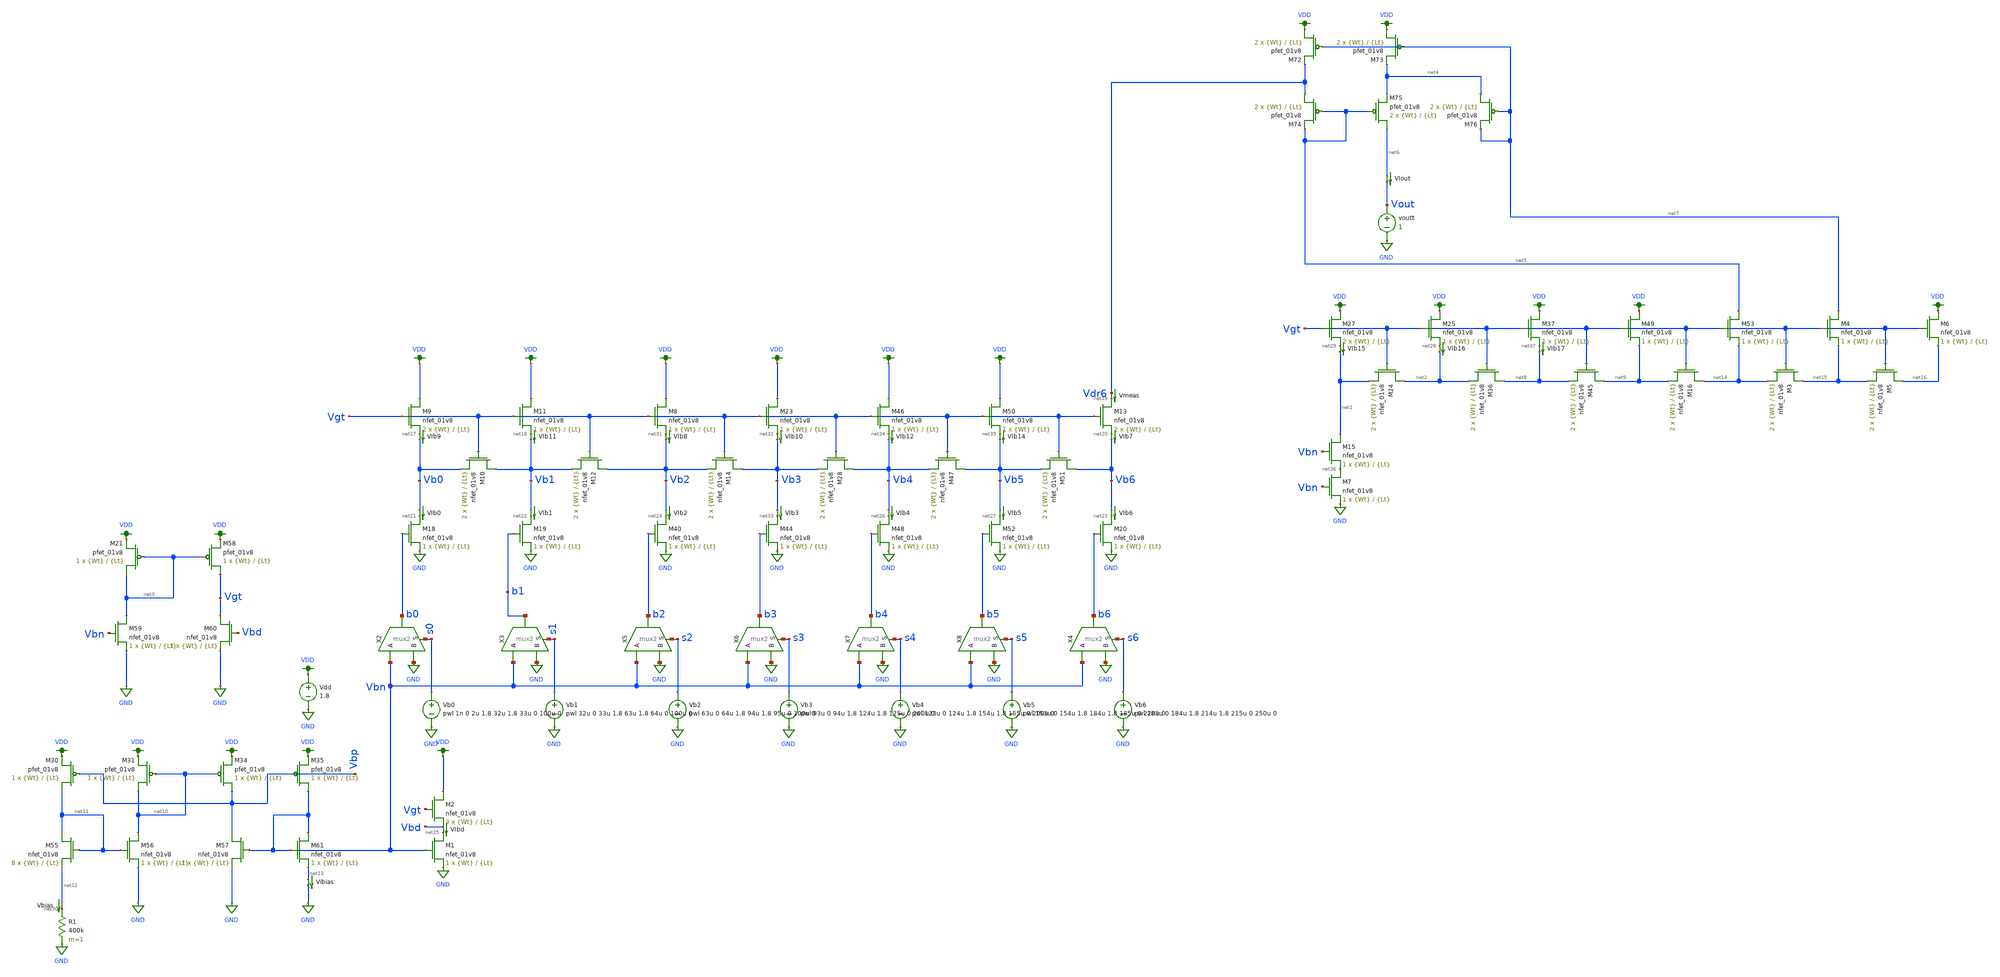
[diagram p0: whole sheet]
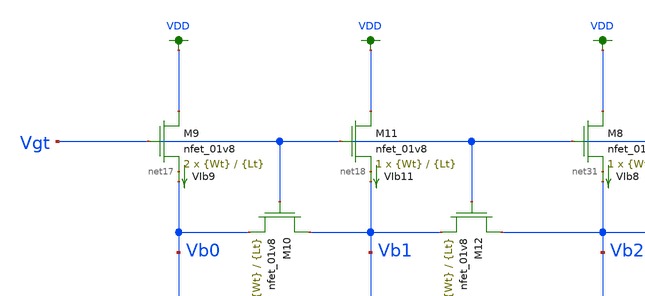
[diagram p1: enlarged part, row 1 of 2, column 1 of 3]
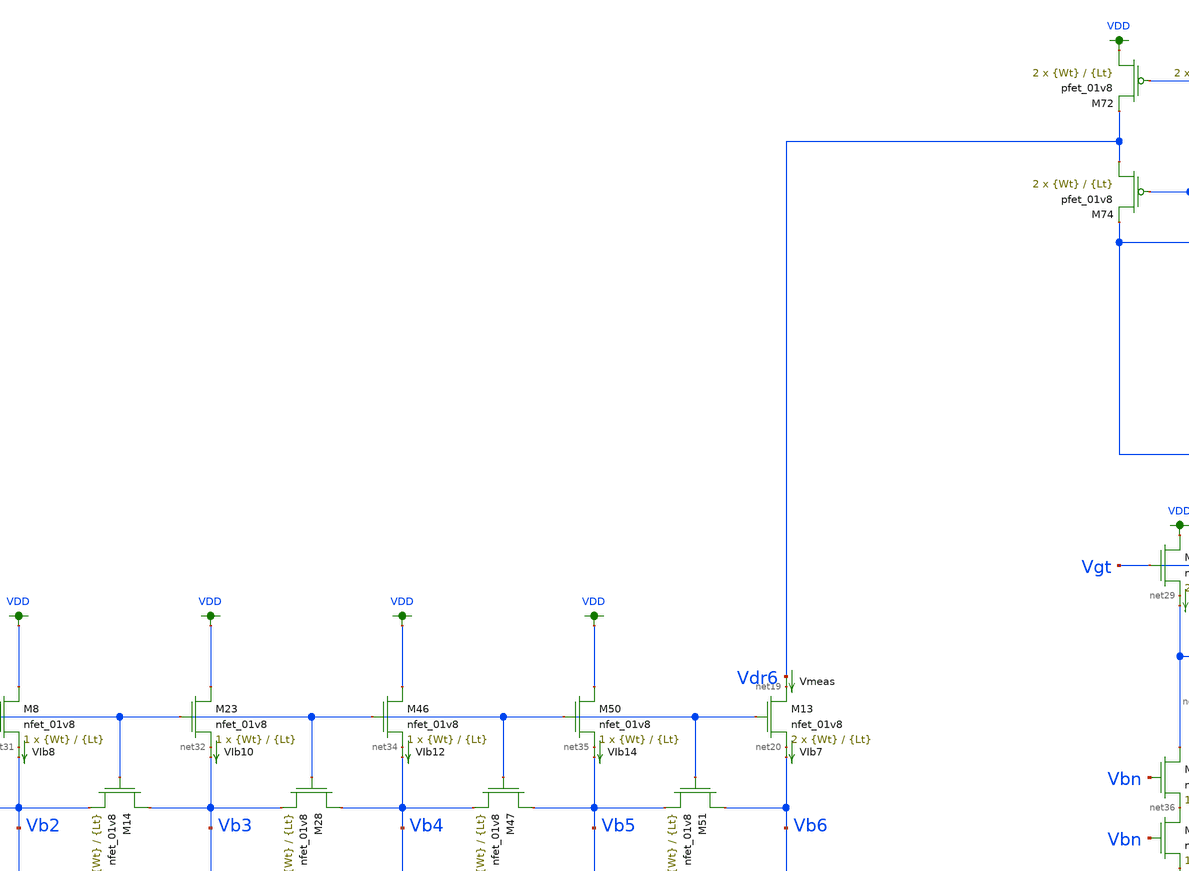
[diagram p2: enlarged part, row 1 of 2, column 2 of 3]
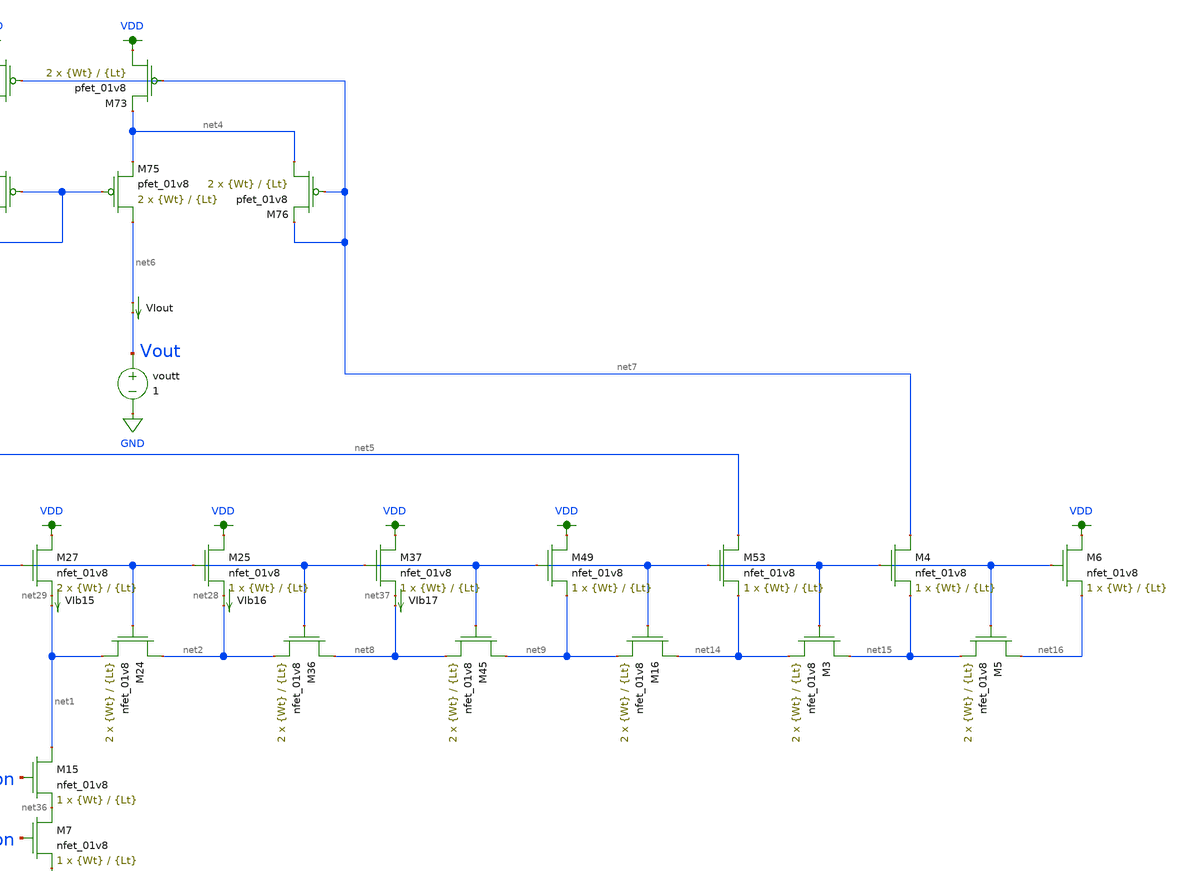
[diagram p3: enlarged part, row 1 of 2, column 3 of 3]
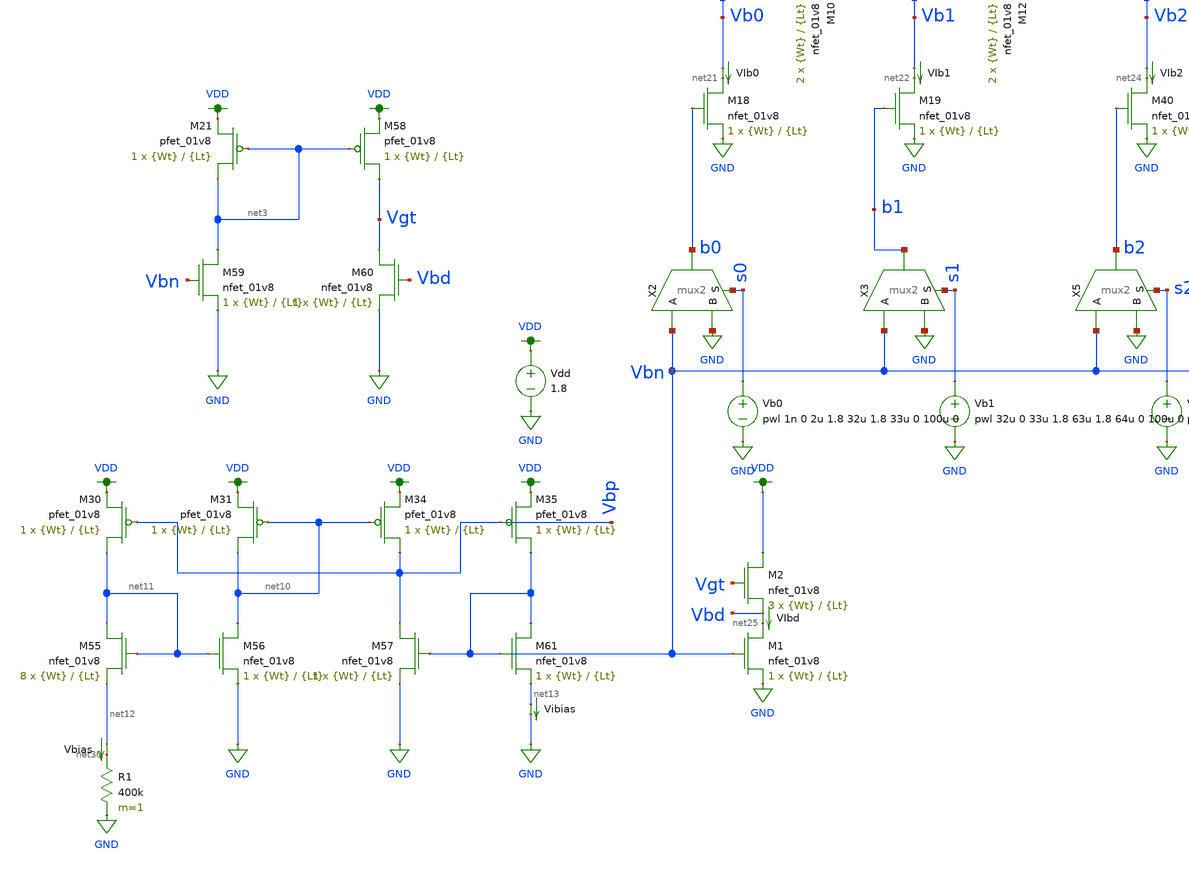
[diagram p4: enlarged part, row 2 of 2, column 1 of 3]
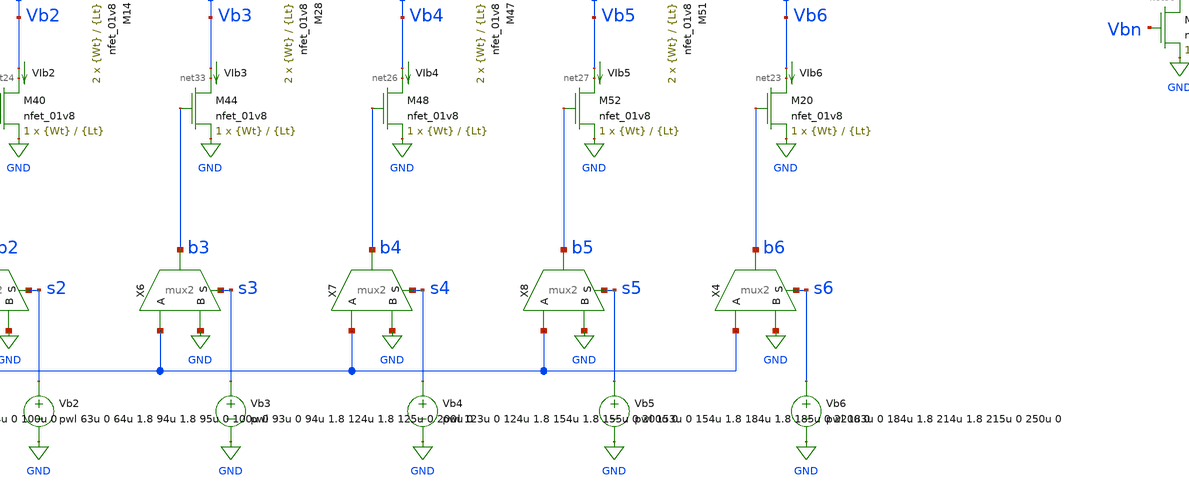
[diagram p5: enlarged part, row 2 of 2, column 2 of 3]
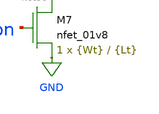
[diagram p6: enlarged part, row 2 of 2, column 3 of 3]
** sch_path: schematic/dac7_test_josh_wilson_idnl.sch
**.subckt dac7_test_josh_wilson_idnl
X2 b0 Vbn GND s0 mux2
X3 b1 Vbn GND s1 mux2
Vdd VDD GND 1.8
Vb0 s0 GND pwl 1n 0 2u 1.8 32u 1.8 33u 0 100u 0
Vb1 s1 GND pwl 32u 0 33u 1.8 63u 1.8 64u 0 100u 0
Vb2 s2 GND pwl 63u 0 64u 1.8 94u 1.8 95u 0 100u 0
XM9 VDD Vgt net17 GND sky130_fd_pr__nfet_01v8 L={Lt} W={Wt} nf=1 ad='int((nf+1)/2) * W/nf * 0.29' as='int((nf+2)/2) * W/nf * 0.29'
+ pd='2*int((nf+1)/2) * (W/nf + 0.29)' ps='2*int((nf+2)/2) * (W/nf + 0.29)' nrd='0.29 / W' nrs='0.29 / W'
+ sa=0 sb=0 sd=0 mult=2 m=2
XM10 Vb1 Vgt Vb0 GND sky130_fd_pr__nfet_01v8 L={Lt} W={Wt} nf=1 ad='int((nf+1)/2) * W/nf * 0.29' as='int((nf+2)/2) * W/nf * 0.29'
+ pd='2*int((nf+1)/2) * (W/nf + 0.29)' ps='2*int((nf+2)/2) * (W/nf + 0.29)' nrd='0.29 / W' nrs='0.29 / W'
+ sa=0 sb=0 sd=0 mult=2 m=2
XM11 VDD Vgt net18 GND sky130_fd_pr__nfet_01v8 L={Lt} W={Wt} nf=1 ad='int((nf+1)/2) * W/nf * 0.29' as='int((nf+2)/2) * W/nf * 0.29'
+ pd='2*int((nf+1)/2) * (W/nf + 0.29)' ps='2*int((nf+2)/2) * (W/nf + 0.29)' nrd='0.29 / W' nrs='0.29 / W'
+ sa=0 sb=0 sd=0 mult=1 m=1
XM12 Vb2 Vgt Vb1 GND sky130_fd_pr__nfet_01v8 L={Lt} W={Wt} nf=1 ad='int((nf+1)/2) * W/nf * 0.29' as='int((nf+2)/2) * W/nf * 0.29'
+ pd='2*int((nf+1)/2) * (W/nf + 0.29)' ps='2*int((nf+2)/2) * (W/nf + 0.29)' nrd='0.29 / W' nrs='0.29 / W'
+ sa=0 sb=0 sd=0 mult=2 m=2
XM13 net19 Vgt net20 GND sky130_fd_pr__nfet_01v8 L={Lt} W={Wt} nf=1 ad='int((nf+1)/2) * W/nf * 0.29'
+ as='int((nf+2)/2) * W/nf * 0.29' pd='2*int((nf+1)/2) * (W/nf + 0.29)' ps='2*int((nf+2)/2) * (W/nf + 0.29)'
+ nrd='0.29 / W' nrs='0.29 / W' sa=0 sb=0 sd=0 mult=2 m=2
XM18 net21 b0 GND GND sky130_fd_pr__nfet_01v8 L={Lt} W={Wt} nf=1 ad='int((nf+1)/2) * W/nf * 0.29' as='int((nf+2)/2) * W/nf * 0.29'
+ pd='2*int((nf+1)/2) * (W/nf + 0.29)' ps='2*int((nf+2)/2) * (W/nf + 0.29)' nrd='0.29 / W' nrs='0.29 / W'
+ sa=0 sb=0 sd=0 mult=1 m=1
XM19 net22 b1 GND GND sky130_fd_pr__nfet_01v8 L={Lt} W={Wt} nf=1 ad='int((nf+1)/2) * W/nf * 0.29' as='int((nf+2)/2) * W/nf * 0.29'
+ pd='2*int((nf+1)/2) * (W/nf + 0.29)' ps='2*int((nf+2)/2) * (W/nf + 0.29)' nrd='0.29 / W' nrs='0.29 / W'
+ sa=0 sb=0 sd=0 mult=1 m=1
XM20 net23 b6 GND GND sky130_fd_pr__nfet_01v8 L={Lt} W={Wt} nf=1 ad='int((nf+1)/2) * W/nf * 0.29' as='int((nf+2)/2) * W/nf * 0.29'
+ pd='2*int((nf+1)/2) * (W/nf + 0.29)' ps='2*int((nf+2)/2) * (W/nf + 0.29)' nrd='0.29 / W' nrs='0.29 / W'
+ sa=0 sb=0 sd=0 mult=1 m=1
Vmeas Vdr6 net19 0
.save i(vmeas)
VIb0 Vb0 net21 0
.save i(vib0)
VIb1 Vb1 net22 0
.save i(vib1)
VIb2 Vb2 net24 0
.save i(vib2)
XM1 net25 Vbn GND GND sky130_fd_pr__nfet_01v8 L={Lt} W={Wt} nf=1 ad='int((nf+1)/2) * W/nf * 0.29' as='int((nf+2)/2) * W/nf * 0.29'
+ pd='2*int((nf+1)/2) * (W/nf + 0.29)' ps='2*int((nf+2)/2) * (W/nf + 0.29)' nrd='0.29 / W' nrs='0.29 / W'
+ sa=0 sb=0 sd=0 mult=1 m=1
VIbd Vbd net25 0
.save i(vibd)
VIb4 Vb4 net26 0
.save i(vib4)
VIb5 Vb5 net27 0
.save i(vib5)
VIb6 Vb6 net23 0
.save i(vib6)
VIout net6 Vout 0
.save i(viout)
XM24 net2 Vgt net1 GND sky130_fd_pr__nfet_01v8 L={Lt} W={Wt} nf=1 ad='int((nf+1)/2) * W/nf * 0.29' as='int((nf+2)/2) * W/nf * 0.29'
+ pd='2*int((nf+1)/2) * (W/nf + 0.29)' ps='2*int((nf+2)/2) * (W/nf + 0.29)' nrd='0.29 / W' nrs='0.29 / W'
+ sa=0 sb=0 sd=0 mult=2 m=2
XM25 VDD Vgt net28 GND sky130_fd_pr__nfet_01v8 L={Lt} W={Wt} nf=1 ad='int((nf+1)/2) * W/nf * 0.29' as='int((nf+2)/2) * W/nf * 0.29'
+ pd='2*int((nf+1)/2) * (W/nf + 0.29)' ps='2*int((nf+2)/2) * (W/nf + 0.29)' nrd='0.29 / W' nrs='0.29 / W'
+ sa=0 sb=0 sd=0 mult=1 m=1
XM27 VDD Vgt net29 GND sky130_fd_pr__nfet_01v8 L={Lt} W={Wt} nf=1 ad='int((nf+1)/2) * W/nf * 0.29' as='int((nf+2)/2) * W/nf * 0.29'
+ pd='2*int((nf+1)/2) * (W/nf + 0.29)' ps='2*int((nf+2)/2) * (W/nf + 0.29)' nrd='0.29 / W' nrs='0.29 / W'
+ sa=0 sb=0 sd=0 mult=2 m=2
XM2 VDD Vgt Vbd GND sky130_fd_pr__nfet_01v8 L={Lt} W={Wt} nf=1 ad='int((nf+1)/2) * W/nf * 0.29' as='int((nf+2)/2) * W/nf * 0.29'
+ pd='2*int((nf+1)/2) * (W/nf + 0.29)' ps='2*int((nf+2)/2) * (W/nf + 0.29)' nrd='0.29 / W' nrs='0.29 / W'
+ sa=0 sb=0 sd=0 mult=3 m=3
XM21 net3 net3 VDD VDD sky130_fd_pr__pfet_01v8 L={Lt} W={Wt} nf=1 ad='int((nf+1)/2) * W/nf * 0.29' as='int((nf+2)/2) * W/nf * 0.29'
+ pd='2*int((nf+1)/2) * (W/nf + 0.29)' ps='2*int((nf+2)/2) * (W/nf + 0.29)' nrd='0.29 / W' nrs='0.29 / W'
+ sa=0 sb=0 sd=0 mult=1 m=1
XM58 Vgt net3 VDD VDD sky130_fd_pr__pfet_01v8 L={Lt} W={Wt} nf=1 ad='int((nf+1)/2) * W/nf * 0.29' as='int((nf+2)/2) * W/nf * 0.29'
+ pd='2*int((nf+1)/2) * (W/nf + 0.29)' ps='2*int((nf+2)/2) * (W/nf + 0.29)' nrd='0.29 / W' nrs='0.29 / W'
+ sa=0 sb=0 sd=0 mult=1 m=1
XM59 net3 Vbn GND GND sky130_fd_pr__nfet_01v8 L={Lt} W={Wt} nf=1 ad='int((nf+1)/2) * W/nf * 0.29' as='int((nf+2)/2) * W/nf * 0.29'
+ pd='2*int((nf+1)/2) * (W/nf + 0.29)' ps='2*int((nf+2)/2) * (W/nf + 0.29)' nrd='0.29 / W' nrs='0.29 / W'
+ sa=0 sb=0 sd=0 mult=1 m=1
XM60 Vgt Vbd GND GND sky130_fd_pr__nfet_01v8 L={Lt} W={Wt} nf=1 ad='int((nf+1)/2) * W/nf * 0.29' as='int((nf+2)/2) * W/nf * 0.29'
+ pd='2*int((nf+1)/2) * (W/nf + 0.29)' ps='2*int((nf+2)/2) * (W/nf + 0.29)' nrd='0.29 / W' nrs='0.29 / W'
+ sa=0 sb=0 sd=0 mult=1 m=1
XM72 VDD net7 Vdr6 VDD sky130_fd_pr__pfet_01v8 L={Lt} W={Wt} nf=1 ad='int((nf+1)/2) * W/nf * 0.29' as='int((nf+2)/2) * W/nf * 0.29'
+ pd='2*int((nf+1)/2) * (W/nf + 0.29)' ps='2*int((nf+2)/2) * (W/nf + 0.29)' nrd='0.29 / W' nrs='0.29 / W'
+ sa=0 sb=0 sd=0 mult=2 m=2
XM73 VDD net7 net4 VDD sky130_fd_pr__pfet_01v8 L={Lt} W={Wt} nf=1 ad='int((nf+1)/2) * W/nf * 0.29' as='int((nf+2)/2) * W/nf * 0.29'
+ pd='2*int((nf+1)/2) * (W/nf + 0.29)' ps='2*int((nf+2)/2) * (W/nf + 0.29)' nrd='0.29 / W' nrs='0.29 / W'
+ sa=0 sb=0 sd=0 mult=2 m=2
XM74 Vdr6 net5 net5 VDD sky130_fd_pr__pfet_01v8 L={Lt} W={Wt} nf=1 ad='int((nf+1)/2) * W/nf * 0.29' as='int((nf+2)/2) * W/nf * 0.29'
+ pd='2*int((nf+1)/2) * (W/nf + 0.29)' ps='2*int((nf+2)/2) * (W/nf + 0.29)' nrd='0.29 / W' nrs='0.29 / W'
+ sa=0 sb=0 sd=0 mult=2 m=2
XM75 net6 net5 net4 VDD sky130_fd_pr__pfet_01v8 L={Lt} W={Wt} nf=1 ad='int((nf+1)/2) * W/nf * 0.29' as='int((nf+2)/2) * W/nf * 0.29'
+ pd='2*int((nf+1)/2) * (W/nf + 0.29)' ps='2*int((nf+2)/2) * (W/nf + 0.29)' nrd='0.29 / W' nrs='0.29 / W'
+ sa=0 sb=0 sd=0 mult=2 m=2
XM76 net4 net7 net7 VDD sky130_fd_pr__pfet_01v8 L={Lt} W={Wt} nf=1 ad='int((nf+1)/2) * W/nf * 0.29' as='int((nf+2)/2) * W/nf * 0.29'
+ pd='2*int((nf+1)/2) * (W/nf + 0.29)' ps='2*int((nf+2)/2) * (W/nf + 0.29)' nrd='0.29 / W' nrs='0.29 / W'
+ sa=0 sb=0 sd=0 mult=2 m=2
R1 net30 GND 400k m=1
Vbias net12 net30 0
.save i(vbias)
X5 b2 Vbn GND s2 mux2
Vb3 s3 GND pwl 93u 0 94u 1.8 124u 1.8 125u 0 200u 0
XM8 VDD Vgt net31 GND sky130_fd_pr__nfet_01v8 L={Lt} W={Wt} nf=1 ad='int((nf+1)/2) * W/nf * 0.29' as='int((nf+2)/2) * W/nf * 0.29'
+ pd='2*int((nf+1)/2) * (W/nf + 0.29)' ps='2*int((nf+2)/2) * (W/nf + 0.29)' nrd='0.29 / W' nrs='0.29 / W'
+ sa=0 sb=0 sd=0 mult=1 m=1
XM14 Vb3 Vgt Vb2 GND sky130_fd_pr__nfet_01v8 L={Lt} W={Wt} nf=1 ad='int((nf+1)/2) * W/nf * 0.29' as='int((nf+2)/2) * W/nf * 0.29'
+ pd='2*int((nf+1)/2) * (W/nf + 0.29)' ps='2*int((nf+2)/2) * (W/nf + 0.29)' nrd='0.29 / W' nrs='0.29 / W'
+ sa=0 sb=0 sd=0 mult=2 m=2
XM40 net24 b2 GND GND sky130_fd_pr__nfet_01v8 L={Lt} W={Wt} nf=1 ad='int((nf+1)/2) * W/nf * 0.29' as='int((nf+2)/2) * W/nf * 0.29'
+ pd='2*int((nf+1)/2) * (W/nf + 0.29)' ps='2*int((nf+2)/2) * (W/nf + 0.29)' nrd='0.29 / W' nrs='0.29 / W'
+ sa=0 sb=0 sd=0 mult=1 m=1
VIb7 net20 Vb6 0
.save i(vib7)
VIb8 net31 Vb2 0
.save i(vib8)
X6 b3 Vbn GND s3 mux2
Vb4 s4 GND pwl 123u 0 124u 1.8 154u 1.8 155u 0 200u 0
XM23 VDD Vgt net32 GND sky130_fd_pr__nfet_01v8 L={Lt} W={Wt} nf=1 ad='int((nf+1)/2) * W/nf * 0.29' as='int((nf+2)/2) * W/nf * 0.29'
+ pd='2*int((nf+1)/2) * (W/nf + 0.29)' ps='2*int((nf+2)/2) * (W/nf + 0.29)' nrd='0.29 / W' nrs='0.29 / W'
+ sa=0 sb=0 sd=0 mult=1 m=1
XM28 Vb4 Vgt Vb3 GND sky130_fd_pr__nfet_01v8 L={Lt} W={Wt} nf=1 ad='int((nf+1)/2) * W/nf * 0.29' as='int((nf+2)/2) * W/nf * 0.29'
+ pd='2*int((nf+1)/2) * (W/nf + 0.29)' ps='2*int((nf+2)/2) * (W/nf + 0.29)' nrd='0.29 / W' nrs='0.29 / W'
+ sa=0 sb=0 sd=0 mult=2 m=2
XM44 net33 b3 GND GND sky130_fd_pr__nfet_01v8 L={Lt} W={Wt} nf=1 ad='int((nf+1)/2) * W/nf * 0.29' as='int((nf+2)/2) * W/nf * 0.29'
+ pd='2*int((nf+1)/2) * (W/nf + 0.29)' ps='2*int((nf+2)/2) * (W/nf + 0.29)' nrd='0.29 / W' nrs='0.29 / W'
+ sa=0 sb=0 sd=0 mult=1 m=1
VIb3 Vb3 net33 0
.save i(vib3)
VIb10 net32 Vb3 0
.save i(vib10)
X7 b4 Vbn GND s4 mux2
Vb5 s5 GND pwl 153u 0 154u 1.8 184u 1.8 185u 0 220u 0
XM46 VDD Vgt net34 GND sky130_fd_pr__nfet_01v8 L={Lt} W={Wt} nf=1 ad='int((nf+1)/2) * W/nf * 0.29' as='int((nf+2)/2) * W/nf * 0.29'
+ pd='2*int((nf+1)/2) * (W/nf + 0.29)' ps='2*int((nf+2)/2) * (W/nf + 0.29)' nrd='0.29 / W' nrs='0.29 / W'
+ sa=0 sb=0 sd=0 mult=1 m=1
XM47 Vb5 Vgt Vb4 GND sky130_fd_pr__nfet_01v8 L={Lt} W={Wt} nf=1 ad='int((nf+1)/2) * W/nf * 0.29' as='int((nf+2)/2) * W/nf * 0.29'
+ pd='2*int((nf+1)/2) * (W/nf + 0.29)' ps='2*int((nf+2)/2) * (W/nf + 0.29)' nrd='0.29 / W' nrs='0.29 / W'
+ sa=0 sb=0 sd=0 mult=2 m=2
XM48 net26 b4 GND GND sky130_fd_pr__nfet_01v8 L={Lt} W={Wt} nf=1 ad='int((nf+1)/2) * W/nf * 0.29' as='int((nf+2)/2) * W/nf * 0.29'
+ pd='2*int((nf+1)/2) * (W/nf + 0.29)' ps='2*int((nf+2)/2) * (W/nf + 0.29)' nrd='0.29 / W' nrs='0.29 / W'
+ sa=0 sb=0 sd=0 mult=1 m=1
VIb9 net17 Vb0 0
.save i(vib9)
VIb12 net34 Vb4 0
.save i(vib12)
X8 b5 Vbn GND s5 mux2
XM50 VDD Vgt net35 GND sky130_fd_pr__nfet_01v8 L={Lt} W={Wt} nf=1 ad='int((nf+1)/2) * W/nf * 0.29' as='int((nf+2)/2) * W/nf * 0.29'
+ pd='2*int((nf+1)/2) * (W/nf + 0.29)' ps='2*int((nf+2)/2) * (W/nf + 0.29)' nrd='0.29 / W' nrs='0.29 / W'
+ sa=0 sb=0 sd=0 mult=1 m=1
XM51 Vb6 Vgt Vb5 GND sky130_fd_pr__nfet_01v8 L={Lt} W={Wt} nf=1 ad='int((nf+1)/2) * W/nf * 0.29' as='int((nf+2)/2) * W/nf * 0.29'
+ pd='2*int((nf+1)/2) * (W/nf + 0.29)' ps='2*int((nf+2)/2) * (W/nf + 0.29)' nrd='0.29 / W' nrs='0.29 / W'
+ sa=0 sb=0 sd=0 mult=2 m=2
XM52 net27 b5 GND GND sky130_fd_pr__nfet_01v8 L={Lt} W={Wt} nf=1 ad='int((nf+1)/2) * W/nf * 0.29' as='int((nf+2)/2) * W/nf * 0.29'
+ pd='2*int((nf+1)/2) * (W/nf + 0.29)' ps='2*int((nf+2)/2) * (W/nf + 0.29)' nrd='0.29 / W' nrs='0.29 / W'
+ sa=0 sb=0 sd=0 mult=1 m=1
VIb11 net18 Vb1 0
.save i(vib11)
VIb14 net35 Vb5 0
.save i(vib14)
Vb6 s6 GND pwl 183u 0 184u 1.8 214u 1.8 215u 0 250u 0
X4 b6 Vbn GND s6 mux2
XM15 net1 Vbn net36 GND sky130_fd_pr__nfet_01v8 L={Lt} W={Wt} nf=1 ad='int((nf+1)/2) * W/nf * 0.29' as='int((nf+2)/2) * W/nf * 0.29'
+ pd='2*int((nf+1)/2) * (W/nf + 0.29)' ps='2*int((nf+2)/2) * (W/nf + 0.29)' nrd='0.29 / W' nrs='0.29 / W'
+ sa=0 sb=0 sd=0 mult=1 m=1
XM36 net8 Vgt net2 GND sky130_fd_pr__nfet_01v8 L={Lt} W={Wt} nf=1 ad='int((nf+1)/2) * W/nf * 0.29' as='int((nf+2)/2) * W/nf * 0.29'
+ pd='2*int((nf+1)/2) * (W/nf + 0.29)' ps='2*int((nf+2)/2) * (W/nf + 0.29)' nrd='0.29 / W' nrs='0.29 / W'
+ sa=0 sb=0 sd=0 mult=2 m=2
XM37 VDD Vgt net37 GND sky130_fd_pr__nfet_01v8 L={Lt} W={Wt} nf=1 ad='int((nf+1)/2) * W/nf * 0.29' as='int((nf+2)/2) * W/nf * 0.29'
+ pd='2*int((nf+1)/2) * (W/nf + 0.29)' ps='2*int((nf+2)/2) * (W/nf + 0.29)' nrd='0.29 / W' nrs='0.29 / W'
+ sa=0 sb=0 sd=0 mult=1 m=1
VIb15 net29 net1 0
.save i(vib15)
VIb16 net28 net2 0
.save i(vib16)
VIb17 net37 net8 0
.save i(vib17)
XM45 net9 Vgt net8 GND sky130_fd_pr__nfet_01v8 L={Lt} W={Wt} nf=1 ad='int((nf+1)/2) * W/nf * 0.29' as='int((nf+2)/2) * W/nf * 0.29'
+ pd='2*int((nf+1)/2) * (W/nf + 0.29)' ps='2*int((nf+2)/2) * (W/nf + 0.29)' nrd='0.29 / W' nrs='0.29 / W'
+ sa=0 sb=0 sd=0 mult=2 m=2
XM49 VDD Vgt net9 GND sky130_fd_pr__nfet_01v8 L={Lt} W={Wt} nf=1 ad='int((nf+1)/2) * W/nf * 0.29' as='int((nf+2)/2) * W/nf * 0.29'
+ pd='2*int((nf+1)/2) * (W/nf + 0.29)' ps='2*int((nf+2)/2) * (W/nf + 0.29)' nrd='0.29 / W' nrs='0.29 / W'
+ sa=0 sb=0 sd=0 mult=1 m=1
XM30 net11 Vbp VDD VDD sky130_fd_pr__pfet_01v8 L={Lt} W={Wt} nf=1 ad='int((nf+1)/2) * W/nf * 0.29' as='int((nf+2)/2) * W/nf * 0.29'
+ pd='2*int((nf+1)/2) * (W/nf + 0.29)' ps='2*int((nf+2)/2) * (W/nf + 0.29)' nrd='0.29 / W' nrs='0.29 / W'
+ sa=0 sb=0 sd=0 mult=1 m=1
XM31 net10 net10 VDD VDD sky130_fd_pr__pfet_01v8 L={Lt} W={Wt} nf=1 ad='int((nf+1)/2) * W/nf * 0.29'
+ as='int((nf+2)/2) * W/nf * 0.29' pd='2*int((nf+1)/2) * (W/nf + 0.29)' ps='2*int((nf+2)/2) * (W/nf + 0.29)'
+ nrd='0.29 / W' nrs='0.29 / W' sa=0 sb=0 sd=0 mult=1 m=1
XM34 Vbp net10 VDD VDD sky130_fd_pr__pfet_01v8 L={Lt} W={Wt} nf=1 ad='int((nf+1)/2) * W/nf * 0.29' as='int((nf+2)/2) * W/nf * 0.29'
+ pd='2*int((nf+1)/2) * (W/nf + 0.29)' ps='2*int((nf+2)/2) * (W/nf + 0.29)' nrd='0.29 / W' nrs='0.29 / W'
+ sa=0 sb=0 sd=0 mult=1 m=1
XM35 Vbn Vbp VDD VDD sky130_fd_pr__pfet_01v8 L={Lt} W={Wt} nf=1 ad='int((nf+1)/2) * W/nf * 0.29' as='int((nf+2)/2) * W/nf * 0.29'
+ pd='2*int((nf+1)/2) * (W/nf + 0.29)' ps='2*int((nf+2)/2) * (W/nf + 0.29)' nrd='0.29 / W' nrs='0.29 / W'
+ sa=0 sb=0 sd=0 mult=1 m=1
XM55 net11 net11 net12 GND sky130_fd_pr__nfet_01v8 L={Lt} W={Wt} nf=1 ad='int((nf+1)/2) * W/nf * 0.29'
+ as='int((nf+2)/2) * W/nf * 0.29' pd='2*int((nf+1)/2) * (W/nf + 0.29)' ps='2*int((nf+2)/2) * (W/nf + 0.29)'
+ nrd='0.29 / W' nrs='0.29 / W' sa=0 sb=0 sd=0 mult=8 m=8
XM56 net10 net11 GND GND sky130_fd_pr__nfet_01v8 L={Lt} W={Wt} nf=1 ad='int((nf+1)/2) * W/nf * 0.29'
+ as='int((nf+2)/2) * W/nf * 0.29' pd='2*int((nf+1)/2) * (W/nf + 0.29)' ps='2*int((nf+2)/2) * (W/nf + 0.29)'
+ nrd='0.29 / W' nrs='0.29 / W' sa=0 sb=0 sd=0 mult=1 m=1
XM57 Vbp Vbn GND GND sky130_fd_pr__nfet_01v8 L={Lt} W={Wt} nf=1 ad='int((nf+1)/2) * W/nf * 0.29' as='int((nf+2)/2) * W/nf * 0.29'
+ pd='2*int((nf+1)/2) * (W/nf + 0.29)' ps='2*int((nf+2)/2) * (W/nf + 0.29)' nrd='0.29 / W' nrs='0.29 / W'
+ sa=0 sb=0 sd=0 mult=1 m=1
XM61 Vbn Vbn net13 GND sky130_fd_pr__nfet_01v8 L={Lt} W={Wt} nf=1 ad='int((nf+1)/2) * W/nf * 0.29' as='int((nf+2)/2) * W/nf * 0.29'
+ pd='2*int((nf+1)/2) * (W/nf + 0.29)' ps='2*int((nf+2)/2) * (W/nf + 0.29)' nrd='0.29 / W' nrs='0.29 / W'
+ sa=0 sb=0 sd=0 mult=1 m=1
Vibias net13 GND 0
.save i(vibias)
voutt Vout GND 1
XM16 net14 Vgt net9 GND sky130_fd_pr__nfet_01v8 L={Lt} W={Wt} nf=1 ad='int((nf+1)/2) * W/nf * 0.29' as='int((nf+2)/2) * W/nf * 0.29'
+ pd='2*int((nf+1)/2) * (W/nf + 0.29)' ps='2*int((nf+2)/2) * (W/nf + 0.29)' nrd='0.29 / W' nrs='0.29 / W'
+ sa=0 sb=0 sd=0 mult=2 m=2
XM53 net5 Vgt net14 GND sky130_fd_pr__nfet_01v8 L={Lt} W={Wt} nf=1 ad='int((nf+1)/2) * W/nf * 0.29' as='int((nf+2)/2) * W/nf * 0.29'
+ pd='2*int((nf+1)/2) * (W/nf + 0.29)' ps='2*int((nf+2)/2) * (W/nf + 0.29)' nrd='0.29 / W' nrs='0.29 / W'
+ sa=0 sb=0 sd=0 mult=1 m=1
XM3 net15 Vgt net14 GND sky130_fd_pr__nfet_01v8 L={Lt} W={Wt} nf=1 ad='int((nf+1)/2) * W/nf * 0.29' as='int((nf+2)/2) * W/nf * 0.29'
+ pd='2*int((nf+1)/2) * (W/nf + 0.29)' ps='2*int((nf+2)/2) * (W/nf + 0.29)' nrd='0.29 / W' nrs='0.29 / W'
+ sa=0 sb=0 sd=0 mult=2 m=2
XM4 net7 Vgt net15 GND sky130_fd_pr__nfet_01v8 L={Lt} W={Wt} nf=1 ad='int((nf+1)/2) * W/nf * 0.29' as='int((nf+2)/2) * W/nf * 0.29'
+ pd='2*int((nf+1)/2) * (W/nf + 0.29)' ps='2*int((nf+2)/2) * (W/nf + 0.29)' nrd='0.29 / W' nrs='0.29 / W'
+ sa=0 sb=0 sd=0 mult=1 m=1
XM5 net16 Vgt net15 GND sky130_fd_pr__nfet_01v8 L={Lt} W={Wt} nf=1 ad='int((nf+1)/2) * W/nf * 0.29' as='int((nf+2)/2) * W/nf * 0.29'
+ pd='2*int((nf+1)/2) * (W/nf + 0.29)' ps='2*int((nf+2)/2) * (W/nf + 0.29)' nrd='0.29 / W' nrs='0.29 / W'
+ sa=0 sb=0 sd=0 mult=2 m=2
XM6 VDD Vgt net16 GND sky130_fd_pr__nfet_01v8 L={Lt} W={Wt} nf=1 ad='int((nf+1)/2) * W/nf * 0.29' as='int((nf+2)/2) * W/nf * 0.29'
+ pd='2*int((nf+1)/2) * (W/nf + 0.29)' ps='2*int((nf+2)/2) * (W/nf + 0.29)' nrd='0.29 / W' nrs='0.29 / W'
+ sa=0 sb=0 sd=0 mult=1 m=1
XM7 net36 Vbn GND GND sky130_fd_pr__nfet_01v8 L={Lt} W={Wt} nf=1 ad='int((nf+1)/2) * W/nf * 0.29' as='int((nf+2)/2) * W/nf * 0.29'
+ pd='2*int((nf+1)/2) * (W/nf + 0.29)' ps='2*int((nf+2)/2) * (W/nf + 0.29)' nrd='0.29 / W' nrs='0.29 / W'
+ sa=0 sb=0 sd=0 mult=1 m=1
**** begin user architecture code

.option wnflag=1
.param MC_SWITCH=1.0
.lib ~/skywater/skywater-pdk/libraries/sky130_fd_pr_ngspice/latest/models/sky130.lib.spice tt


.param Wt = 30
.param Lt = 6
.control
*** change W and L for the next two lines as well !***
  let myW = 30
  let myL = 6
  set wr_singlescale
  let runs = 3
  let run = 1
  while run <= runs
    set appendwrite = FALSE
    set wr_vecnames
    let code = 0
    while code < 128
      if code eq 0
        let b0 = 0
      else
        let b0 = (code % 2) * 1.8
      end
      if floor(code / 2) eq 0
        let b1 = 0
      else
        let b1 = (floor(code / 2) % 2) * 1.8
      end
      if floor(code / 4) eq 0
        let b2 = 0
      else
        let b2 = (floor(code / 4) % 2) * 1.8
      end
      if floor(code / 8) eq 0
        let b3 = 0
      else
        let b3 = floor(code / 8) % 2 * 1.8
      end
      if floor(code / 16) eq 0
        let b4 = 0
      else
        let b4 = floor(code / 16) % 2 * 1.8
      end
      if floor(code / 32) eq 0
        let b5 = 0
      else
        let b5 = floor(code / 32) % 2 * 1.8
      end
      if floor(code / 64) eq 0
        let b6 = 0
      else
        let b6 = floor(code / 64) % 2 * 1.8
      end
      alter vb0 $&b0
      alter vb1 $&b1
      alter vb2 $&b2
      alter vb3 $&b3
      alter vb4 $&b4
      alter vb5 $&b5
      alter vb6 $&b6
      save v(b0) v(b1) v(b2) v(b3) v(b4) v(b5) v(b6) i(vbias) i(viout) v(vout)
      op
      wrdata ~/Documents/MADVLSI-MP4/schematic/data/dac7mc_L{$&myL}W{$&myW}op-{$&run}.txt v(b0) v(b1)
+ v(b2) v(b3) v(b4) v(b5) v(b6) i(vbias) i(viout) v(vout)
      if code eq 0
        set appendwrite
        set wr_vecnames = FALSE
      end
      let code = code + 1
    end
    reset
    let run = run + 1
  end

  set appendwrite = FALSE
  reset
  set wr_singlescale
  set wr_vecnames
  alter vb0 1.8
  alter vb1 1.8
  alter vb2 1.8
  alter vb3 1.8
  alter vb4 1.8
  alter vb5 1.8
  alter vb6 1.8
  save v(b0) v(b1) v(b2) v(b3) v(b4) v(b5) v(b6) i(vbias) i(viout) v(vout)
  dc Voutt 0 1.8 0.01
  run
  wrdata ~/Documents/MADVLSI-MP4/schematic/data/dac7mc_L{$&myL}W{$&myW}vout-1.txt v(b0) v(b1) v(b2) v(b3)
+ v(b4) v(b5) v(b6) i(vbias) i(viout) v(vout)

  reset
  set wr_singlescale
  set wr_vecnames
  alter vb0 1.8
  alter vb1 1.8
  alter vb2 1.8
  alter vb3 1.8
  alter vb4 1.8
  alter vb5 1.8
  alter vb6 0
  save v(b0) v(b1) v(b2) v(b3) v(b4) v(b5) v(b6) i(vbias) i(viout) v(vout)
  dc Voutt 0 1.8 0.01
  run
  wrdata ~/Documents/MADVLSI-MP4/schematic/data/dac7mc_L{$&myL}W{$&myW}vout-2.txt v(b0) v(b1) v(b2) v(b3)
+ v(b4) v(b5) v(b6) i(vbias) i(viout) v(vout)

  reset
  set wr_singlescale
  set wr_vecnames
  alter vb0 1.8
  alter vb1 1.8
  alter vb2 1.8
  alter vb3 1.8
  alter vb4 1.8
  alter vb5 1.8
  alter vb6 1.8
  save v(b0) v(b1) v(b2) v(b3) v(b4) v(b5) v(b6) i(vbias) i(viout) v(vout)
  dc Vdd 0 1.8 0.01
  run
  wrdata ~/Documents/MADVLSI-MP4/schematic/data/dac7mc_L{$&myL}W{$&myW}vdd-1.txt v(b0) v(b1) v(b2) v(b3)
+ v(b4) v(b5) v(b6) i(vbias) i(viout) v(vout)

  reset
  set wr_singlescale
  set wr_vecnames
  alter vb0 1.8
  alter vb1 1.8
  alter vb2 1.8
  alter vb3 1.8
  alter vb4 1.8
  alter vb5 1.8
  alter vb6 0
  save v(b0) v(b1) v(b2) v(b3) v(b4) v(b5) v(b6) i(vbias) i(viout) v(vout)
  dc Vdd 0 1.8 0.01
  run
  wrdata ~/Documents/MADVLSI-MP4/schematic/data/dac7mc_L{$&myL}W{$&myW}vdd-2.txt v(b0) v(b1) v(b2) v(b3)
+ v(b4) v(b5) v(b6) i(vbias) i(viout) v(vout)
.endc

**** end user architecture code
**.ends
.GLOBAL GND
.GLOBAL VDD
.end
